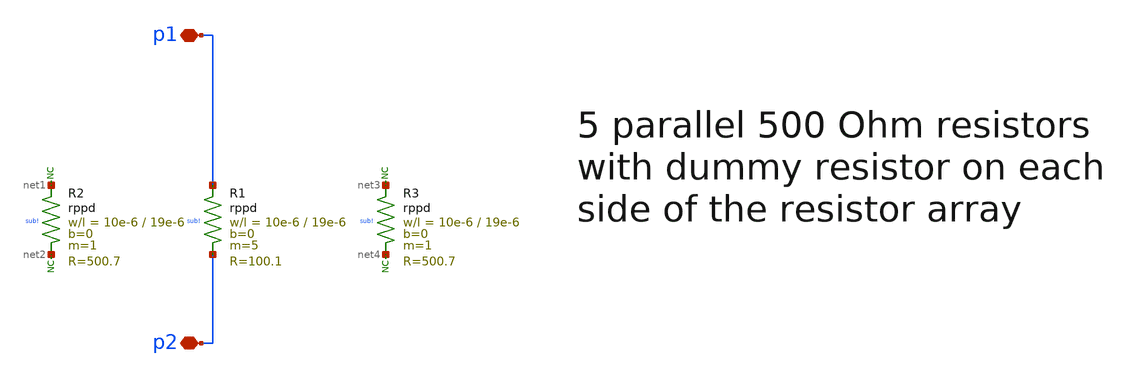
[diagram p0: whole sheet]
** sch_path: LNA0379-main/schematic/xschem/MatchResistorArray.sch
**.subckt MatchResistorArray p1 p2
*.iopin p1
*.iopin p2
XR1 p1 p2 sub! rppd w=10e-6 l=19e-6 m=5 b=0 mm_ok=1
XR2 net1 net2 sub! rppd w=10e-6 l=19e-6 m=1 b=0 mm_ok=1
XR3 net3 net4 sub! rppd w=10e-6 l=19e-6 m=1 b=0 mm_ok=1
* noconn #net1
* noconn #net2
* noconn #net4
* noconn #net3
**.ends
.end
